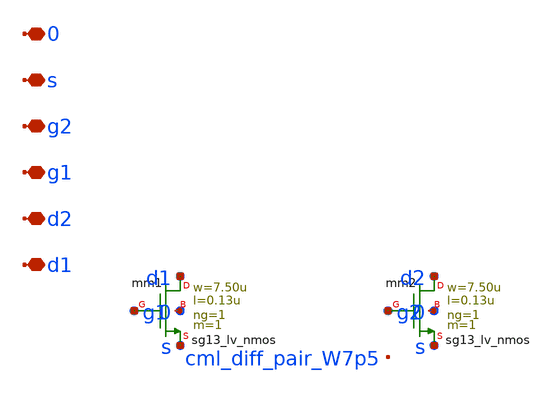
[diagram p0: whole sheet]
** sch_path: analog/lo/sch/cml_diff_pair.sch
**.subckt cml_diff_pair d1 d2 g1 g2 s 0
*.iopin d1
*.iopin d2
*.iopin g1
*.iopin g2
*.iopin s
*.iopin 0
Xmm1 d1 g1 s 0 sg13_lv_nmos w=7.50u l=0.13u ng=1 m=1 mm_ok=1
Xmm2 d2 g2 s 0 sg13_lv_nmos w=7.50u l=0.13u ng=1 m=1 mm_ok=1
**.ends
.end
